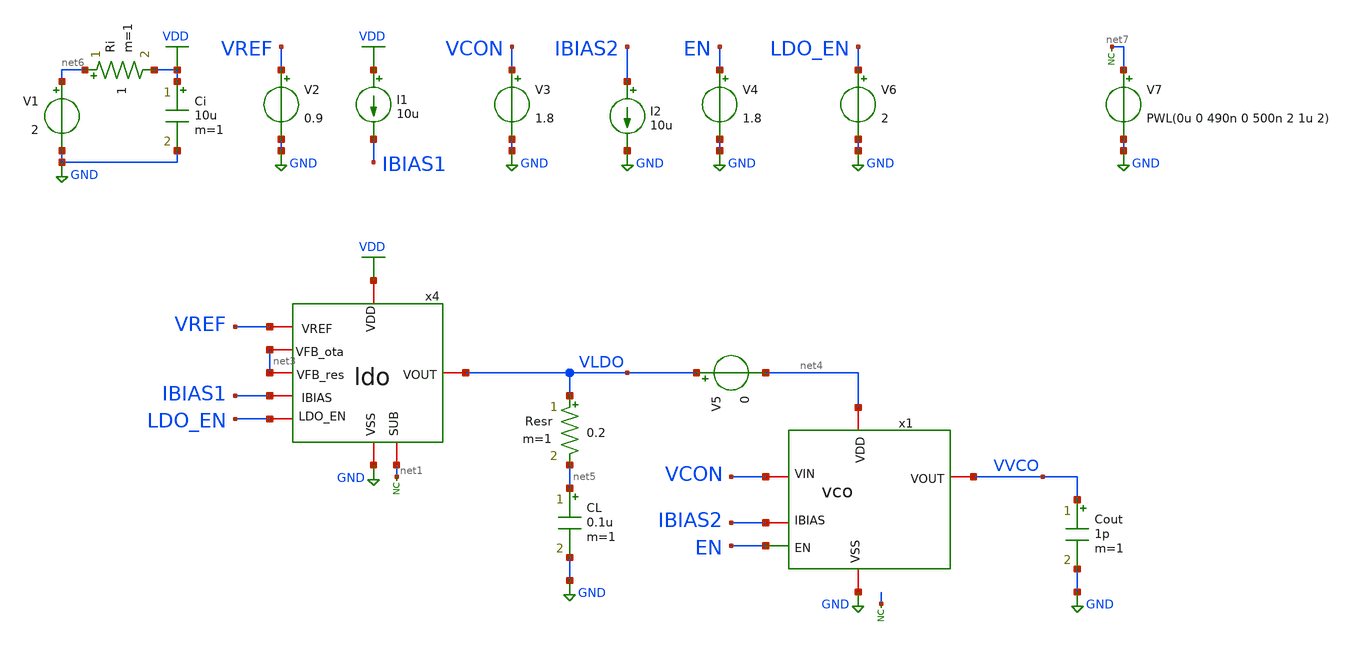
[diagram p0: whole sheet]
** sch_path: designs/libs/tb_top/tb_top_ldo_vco_tran/tb_top_ldo_vco_tran.sch
**.subckt tb_top_ldo_vco_tran
V3 VCON GND 1.8
I2 IBIAS2 GND 10u
V4 EN GND 1.8
x1 net4 IBIAS2 VVCO EN GND VCON vco
x4 VDD VREF VLDO IBIAS1 net1 GND LDO_EN net3 net3 ldo
* noconn #net1
* noconn #net2
V2 VREF GND 0.9
CL net5 GND 0.1u m=1
Resr VLDO net5 0.2 m=1
I1 VDD IBIAS1 10u
Ri net6 VDD 1 m=1
Ci VDD GND 10u m=1
V1 net6 GND 2
V5 VLDO net4 0
Cout VVCO GND 1p m=1
V6 LDO_EN GND 2
V7 net7 GND PWL(0u 0 490n 0 500n 2 1u 2)
* noconn #net7
**** begin user architecture code



.control
save all

run
set color0 = white

** SIMULATIONS
tran 10p 1u 0

** PLOTS
setplot tran1
let vin_ldo = v(VDD)
let vout_ldo = v(VLDO)
let en_vco = v(EN)
let vout_vco = v(VVCO)
plot vout_ldo vin_ldo en_vco
plot vout_vco

** MEASUREMENTS
meas TRAN tdiff TRIG v(VVCO) VAL=0.9 RISE=500 TARG v(VVCO) VAL=0.9 RISE=501
let freq = 1 / tdiff
print freq
let iload = v5#branch
meas tran ivco INTEG iload from=600n to=800n
print ivco
meas tran vdd_vco INTEG vldo from=600n to=800n
print vdd_vco
let pcom_avg = ivco*vdd_vco
print pcom_avg

write tb_top_ldo_vco_tran.raw

.endc
* ngspice commands




.include $::180MCU_MODELS/design.ngspice
.lib $::180MCU_MODELS/sm141064.ngspice typical
.lib $::180MCU_MODELS/sm141064.ngspice cap_mim
.lib $::180MCU_MODELS/sm141064.ngspice moscap_typical
.lib $::180MCU_MODELS/sm141064.ngspice mimcap_typical
.lib $::180MCU_MODELS/sm141064.ngspice res_typical
* .lib $::180MCU_MODELS/sm141064.ngspice res_statistical
* ngspice commands

**** end user architecture code
**.ends
.GLOBAL GND
.GLOBAL VDD
.end
